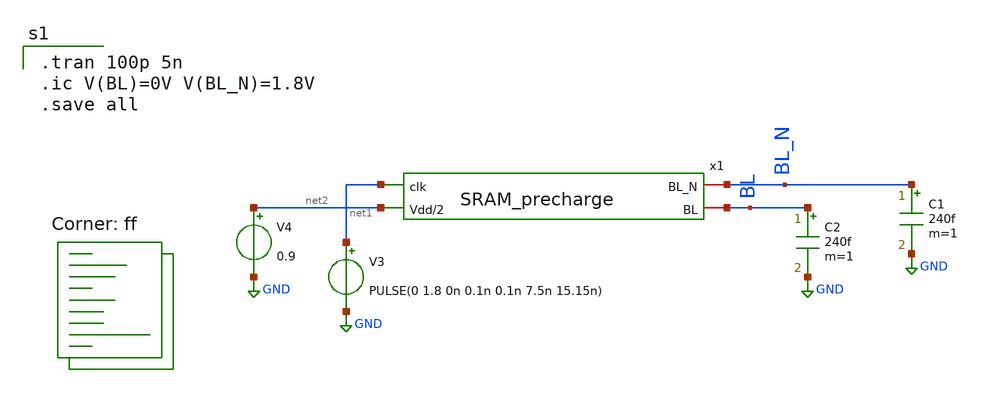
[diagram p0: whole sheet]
** sch_path: analog/schematics/tb.sch
**.subckt tb
x1 BL_N BL net1 net2 SRAM_precharge
C1 BL_N GND 240f m=1
C2 BL GND 240f m=1
V3 net1 GND PULSE(0 1.8 0n 0.1n 0.1n 7.5n 15.15n)
V4 net2 GND 0.9
**** begin user architecture code

.tran 100p 5n
.ic V(BL)=0V V(BL_N)=1.8V
.save all

.lib $::SKYWATER_MODELS/sky130.lib.spice ff
**** end user architecture code
**.ends

* expanding   symbol:  SRAM_precharge.sym # of pins=4
** sym_path: analog/schematics/SRAM_precharge.sym
** sch_path: analog/schematics/SRAM_precharge.sch
.subckt SRAM_precharge BL_N BL clk Vdd/2
*.iopin BL
*.iopin BL_N
*.ipin Vdd/2
*.ipin clk
XM1 BL clk Vdd/2 GND sky130_fd_pr__nfet_01v8 L=0.15 W=10 nf=1 ad='int((nf+1)/2) * W/nf * 0.29' as='int((nf+2)/2) * W/nf * 0.29'
+ pd='2*int((nf+1)/2) * (W/nf + 0.29)' ps='2*int((nf+2)/2) * (W/nf + 0.29)' nrd='0.29 / W' nrs='0.29 / W'
+ sa=0 sb=0 sd=0 mult=1 m=1
XM2 BL_N clk Vdd/2 GND sky130_fd_pr__nfet_01v8 L=0.15 W=10 nf=1 ad='int((nf+1)/2) * W/nf * 0.29' as='int((nf+2)/2) * W/nf * 0.29'
+ pd='2*int((nf+1)/2) * (W/nf + 0.29)' ps='2*int((nf+2)/2) * (W/nf + 0.29)' nrd='0.29 / W' nrs='0.29 / W'
+ sa=0 sb=0 sd=0 mult=1 m=1
XM3 BL clk BL_N GND sky130_fd_pr__nfet_01v8 L=0.15 W=10 nf=1 ad='int((nf+1)/2) * W/nf * 0.29' as='int((nf+2)/2) * W/nf * 0.29'
+ pd='2*int((nf+1)/2) * (W/nf + 0.29)' ps='2*int((nf+2)/2) * (W/nf + 0.29)' nrd='0.29 / W' nrs='0.29 / W'
+ sa=0 sb=0 sd=0 mult=1 m=1
.ends

.GLOBAL GND
.end
